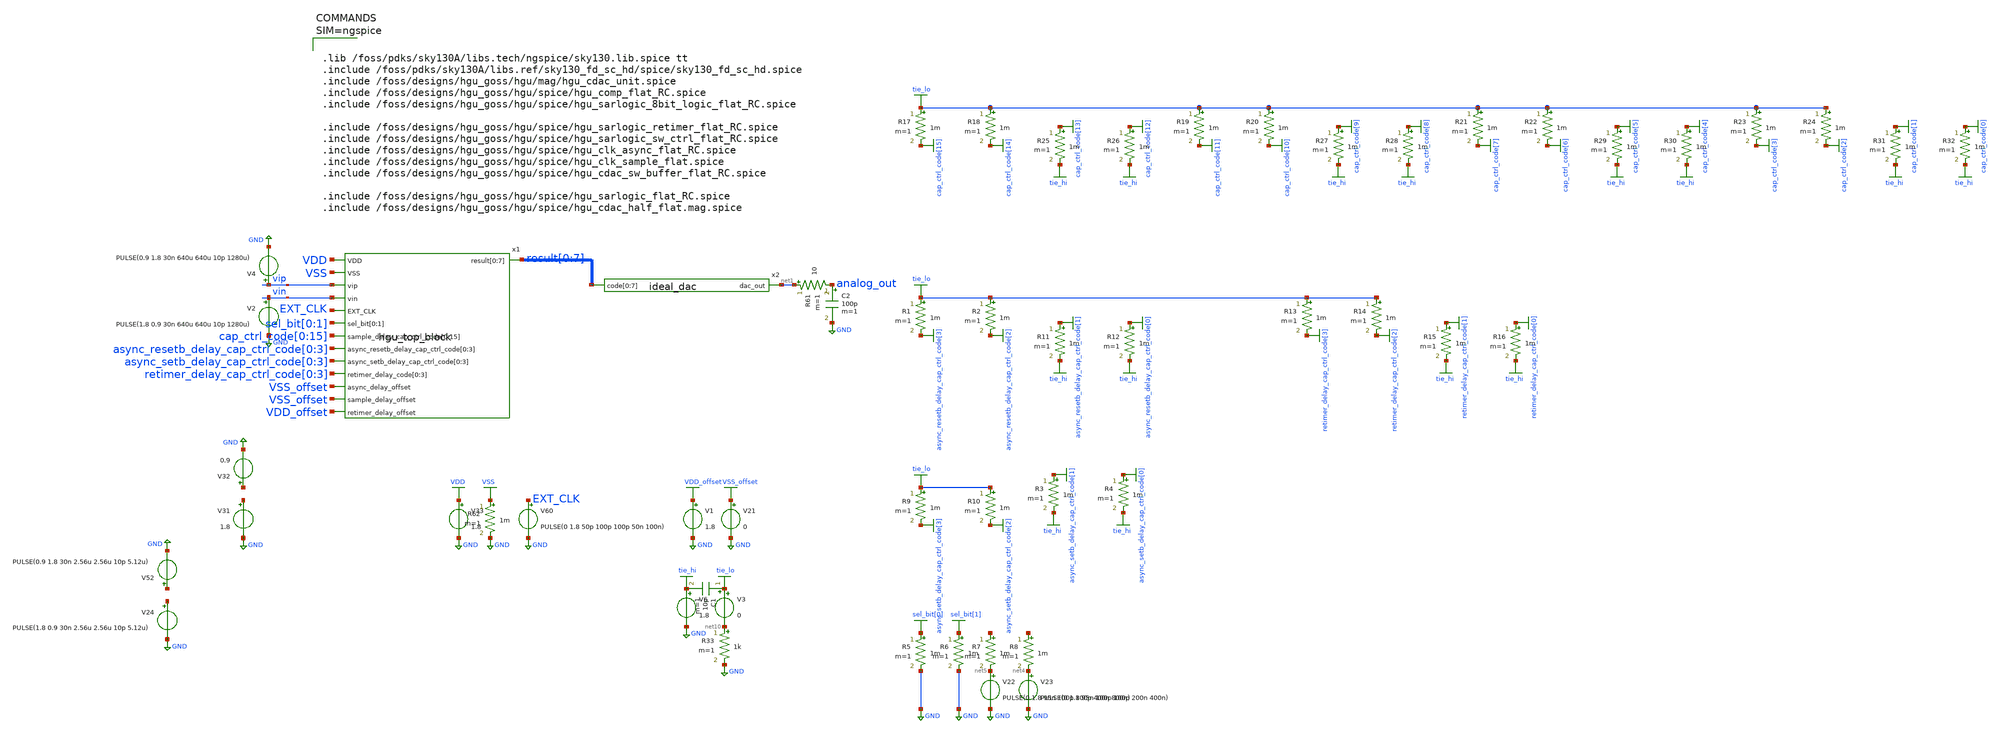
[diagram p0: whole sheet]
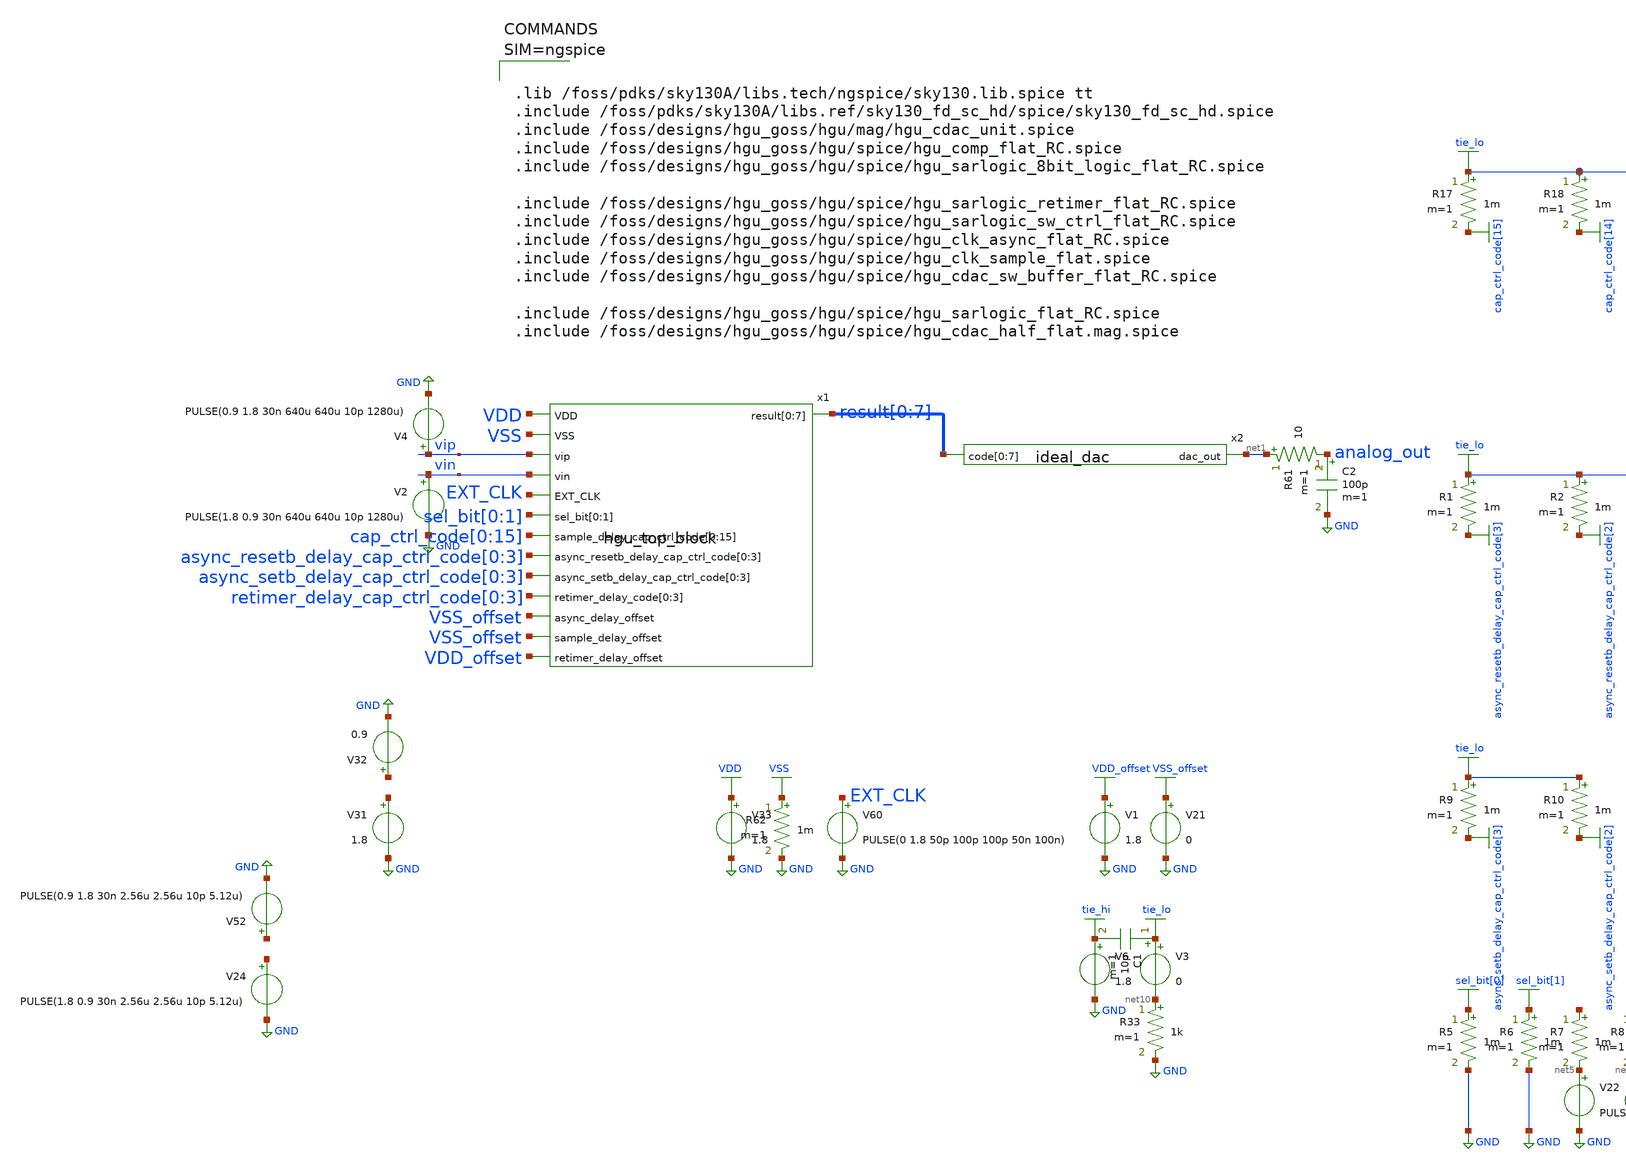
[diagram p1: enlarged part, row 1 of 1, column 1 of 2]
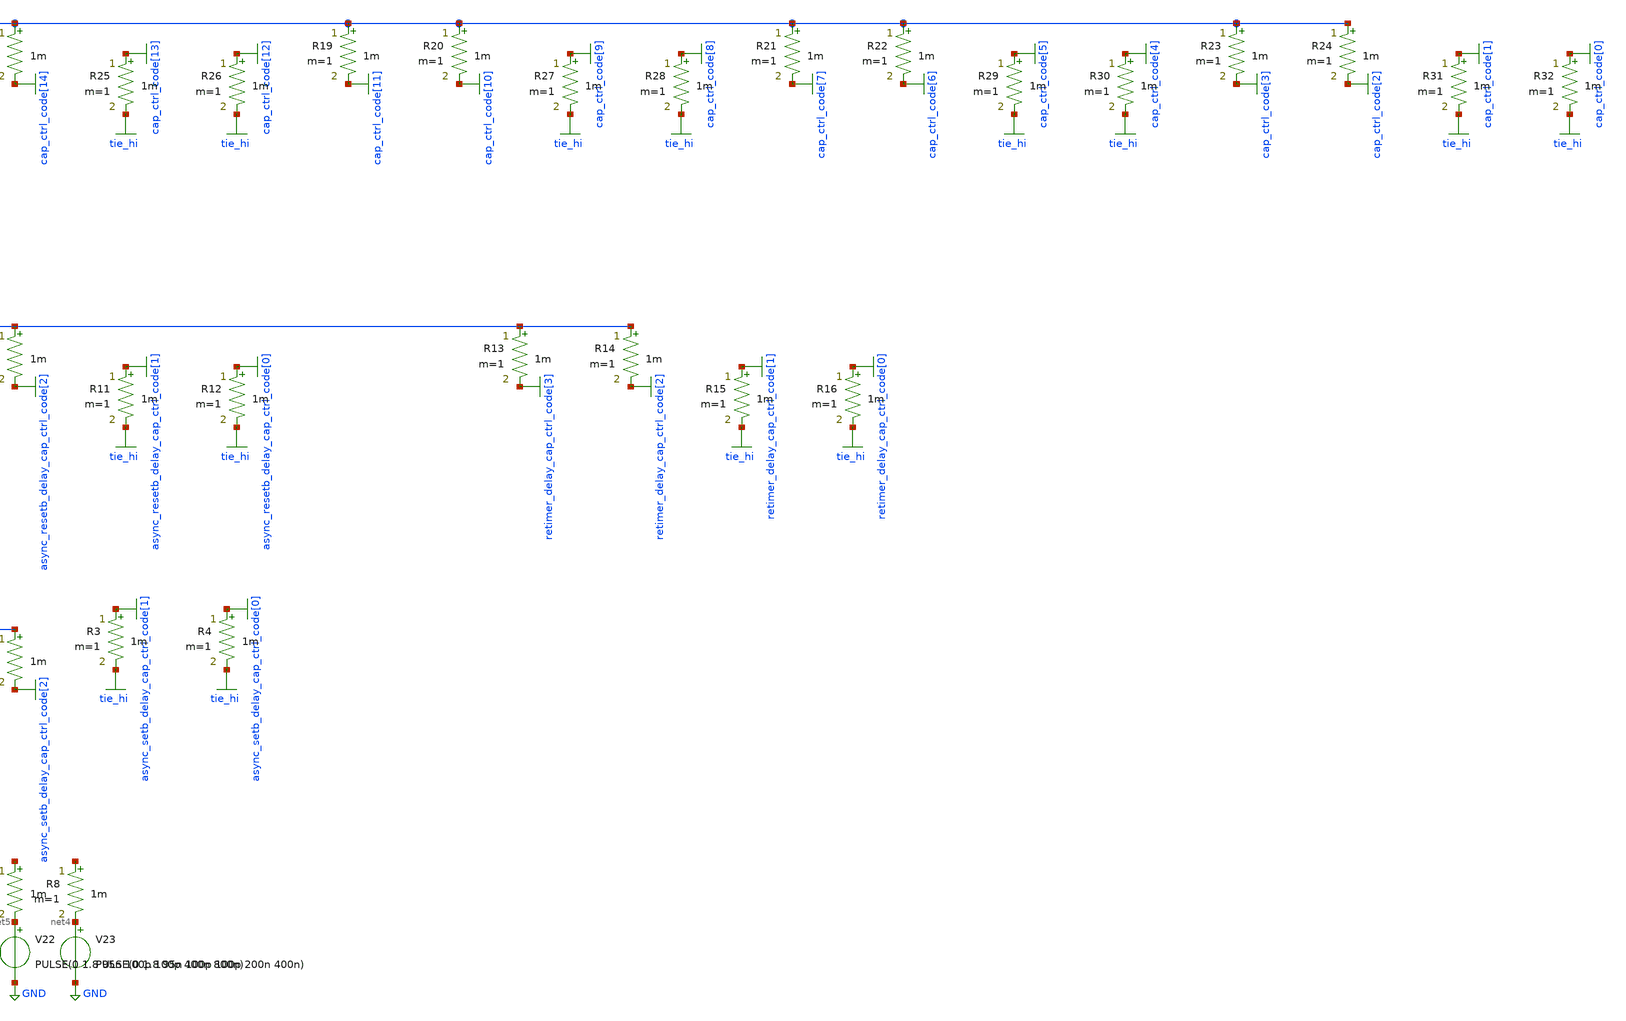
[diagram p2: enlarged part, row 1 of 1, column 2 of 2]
** sch_path: tb/tb_hgu_top_block_batch.sch
**.subckt tb_hgu_top_block_batch
x1 VDD result[0] result[1] result[2] result[3] result[4] result[5] result[6] result[7] VSS vip vin
+ EXT_CLK sel_bit[0] sel_bit[1] cap_ctrl_code[0] cap_ctrl_code[1] cap_ctrl_code[2] cap_ctrl_code[3]
+ cap_ctrl_code[4] cap_ctrl_code[5] cap_ctrl_code[6] cap_ctrl_code[7] cap_ctrl_code[8] cap_ctrl_code[9]
+ cap_ctrl_code[10] cap_ctrl_code[11] cap_ctrl_code[12] cap_ctrl_code[13] cap_ctrl_code[14] cap_ctrl_code[15]
+ async_resetb_delay_cap_ctrl_code[0] async_resetb_delay_cap_ctrl_code[1] async_resetb_delay_cap_ctrl_code[2]
+ async_resetb_delay_cap_ctrl_code[3] async_setb_delay_cap_ctrl_code[0] async_setb_delay_cap_ctrl_code[1]
+ async_setb_delay_cap_ctrl_code[2] async_setb_delay_cap_ctrl_code[3] retimer_delay_cap_ctrl_code[0] retimer_delay_cap_ctrl_code[1]
+ retimer_delay_cap_ctrl_code[2] retimer_delay_cap_ctrl_code[3] VSS_offset VSS_offset VDD_offset hgu_top_block
C2 analog_out GND 100p m=1
V33 VDD GND 1.8
V31 net2 GND 1.8
V32 net3 GND 0.9
V60 EXT_CLK GND PULSE(0 1.8 50p 100p 100p 50n 100n)
V2 vin GND PULSE(1.8 0.9 30n 640u 640u 10p 1280u)
V4 vip GND PULSE(0.9 1.8 30n 640u 640u 10p 1280u)
V1 VDD_offset GND 1.8
V21 VSS_offset GND 0
V23 net4 GND PULSE(0 1.8 95n 100p 100p 200n 400n)
V22 net5 GND PULSE(0 1.8 95n 100p 100p 400n 800n)
x2 net1 result[0] result[1] result[2] result[3] result[4] result[5] result[6] result[7] ideal_dac
V24 net6 GND PULSE(1.8 0.9 30n 2.56u 2.56u 10p 5.12u)
V52 net7 GND PULSE(0.9 1.8 30n 2.56u 2.56u 10p 5.12u)
R61 net1 analog_out 10 m=1
R62 VSS GND 1m m=1
R3 async_setb_delay_cap_ctrl_code[1] tie_hi 1m m=1
R4 async_setb_delay_cap_ctrl_code[0] tie_hi 1m m=1
R5 sel_bit[0] GND 1m m=1
R6 sel_bit[1] GND 1m m=1
R7 net8 net5 1m m=1
R8 net9 net4 1m m=1
V6 tie_hi GND 1.8
R9 tie_lo async_setb_delay_cap_ctrl_code[3] 1m m=1
R10 tie_lo async_setb_delay_cap_ctrl_code[2] 1m m=1
R1 tie_lo async_resetb_delay_cap_ctrl_code[3] 1m m=1
R2 tie_lo async_resetb_delay_cap_ctrl_code[2] 1m m=1
R11 async_resetb_delay_cap_ctrl_code[1] tie_hi 1m m=1
R12 async_resetb_delay_cap_ctrl_code[0] tie_hi 1m m=1
R13 tie_lo retimer_delay_cap_ctrl_code[3] 1m m=1
R14 tie_lo retimer_delay_cap_ctrl_code[2] 1m m=1
R15 retimer_delay_cap_ctrl_code[1] tie_hi 1m m=1
R16 retimer_delay_cap_ctrl_code[0] tie_hi 1m m=1
R17 tie_lo cap_ctrl_code[15] 1m m=1
R18 tie_lo cap_ctrl_code[14] 1m m=1
R19 tie_lo cap_ctrl_code[11] 1m m=1
R20 tie_lo cap_ctrl_code[10] 1m m=1
R21 tie_lo cap_ctrl_code[7] 1m m=1
R22 tie_lo cap_ctrl_code[6] 1m m=1
R23 tie_lo cap_ctrl_code[3] 1m m=1
R24 tie_lo cap_ctrl_code[2] 1m m=1
R25 cap_ctrl_code[13] tie_hi 1m m=1
R26 cap_ctrl_code[12] tie_hi 1m m=1
R27 cap_ctrl_code[9] tie_hi 1m m=1
R28 cap_ctrl_code[8] tie_hi 1m m=1
R29 cap_ctrl_code[5] tie_hi 1m m=1
R30 cap_ctrl_code[4] tie_hi 1m m=1
R31 cap_ctrl_code[1] tie_hi 1m m=1
R32 cap_ctrl_code[0] tie_hi 1m m=1
R33 net10 GND 1k m=1
V3 tie_lo net10 0
C1 tie_lo tie_hi 10p m=1
**** begin user architecture code



.lib /foss/pdks/sky130A/libs.tech/ngspice/sky130.lib.spice tt
.include /foss/pdks/sky130A/libs.ref/sky130_fd_sc_hd/spice/sky130_fd_sc_hd.spice
.include /foss/designs/hgu_goss/hgu/mag/hgu_cdac_unit.spice
.include /foss/designs/hgu_goss/hgu/spice/hgu_comp_flat_RC.spice
.include /foss/designs/hgu_goss/hgu/spice/hgu_sarlogic_8bit_logic_flat_RC.spice

.include /foss/designs/hgu_goss/hgu/spice/hgu_sarlogic_retimer_flat_RC.spice
.include /foss/designs/hgu_goss/hgu/spice/hgu_sarlogic_sw_ctrl_flat_RC.spice
.include /foss/designs/hgu_goss/hgu/spice/hgu_clk_async_flat_RC.spice
.include /foss/designs/hgu_goss/hgu/spice/hgu_clk_sample_flat.spice
.include /foss/designs/hgu_goss/hgu/spice/hgu_cdac_sw_buffer_flat_RC.spice

.include /foss/designs/hgu_goss/hgu/spice/hgu_sarlogic_flat_RC.spice
.include /foss/designs/hgu_goss/hgu/spice/hgu_cdac_half_flat.mag.spice






.tran 10ps 300us

.option ABSTOL=1e-9 RELTOL=1e-2

.save x1.sample_clk vip vin analog_out i(v33)


**** end user architecture code
**.ends
.GLOBAL cap_ctrl_code[15]
.GLOBAL cap_ctrl_code[14]
.GLOBAL cap_ctrl_code[13]
.GLOBAL cap_ctrl_code[12]
.GLOBAL cap_ctrl_code[11]
.GLOBAL cap_ctrl_code[10]
.GLOBAL cap_ctrl_code[9]
.GLOBAL cap_ctrl_code[8]
.GLOBAL GND
.GLOBAL async_resetb_delay_cap_ctrl_code[3]
.GLOBAL async_resetb_delay_cap_ctrl_code[2]
.GLOBAL async_resetb_delay_cap_ctrl_code[1]
.GLOBAL async_resetb_delay_cap_ctrl_code[0]
.GLOBAL async_setb_delay_cap_ctrl_code[3]
.GLOBAL async_setb_delay_cap_ctrl_code[2]
.GLOBAL async_setb_delay_cap_ctrl_code[1]
.GLOBAL async_setb_delay_cap_ctrl_code[0]
.GLOBAL cap_ctrl_code[7]
.GLOBAL cap_ctrl_code[6]
.GLOBAL cap_ctrl_code[5]
.GLOBAL cap_ctrl_code[4]
.GLOBAL cap_ctrl_code[3]
.GLOBAL cap_ctrl_code[2]
.GLOBAL cap_ctrl_code[1]
.GLOBAL cap_ctrl_code[0]
.GLOBAL retimer_delay_cap_ctrl_code[3]
.GLOBAL retimer_delay_cap_ctrl_code[2]
.GLOBAL retimer_delay_cap_ctrl_code[1]
.GLOBAL retimer_delay_cap_ctrl_code[0]
.GLOBAL VDD
.GLOBAL VSS
.GLOBAL VDD_offset
.GLOBAL VSS_offset
.GLOBAL sel_bit[1]
.GLOBAL sel_bit[0]
.GLOBAL tie_hi
.GLOBAL tie_lo
.end
